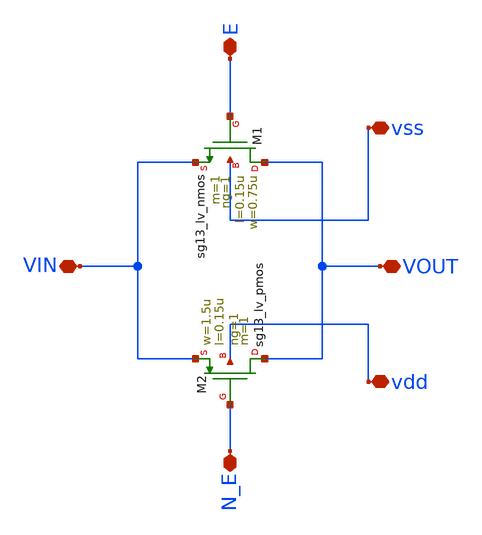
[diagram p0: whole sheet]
** sch_path: design/blocks/tg/schematic/tg.sch
**.subckt tg VOUT E N_E VIN vss vdd
*.iopin VOUT
*.iopin E
*.iopin N_E
*.iopin VIN
*.iopin vss
*.iopin vdd
XM1 VOUT E VIN vss sg13_lv_nmos w=0.75u l=0.15u ng=1 m=1 mm_ok=1
XM2 VOUT N_E VIN vdd sg13_lv_pmos w=1.5u l=0.15u ng=1 m=1 mm_ok=1
**.ends
.end
